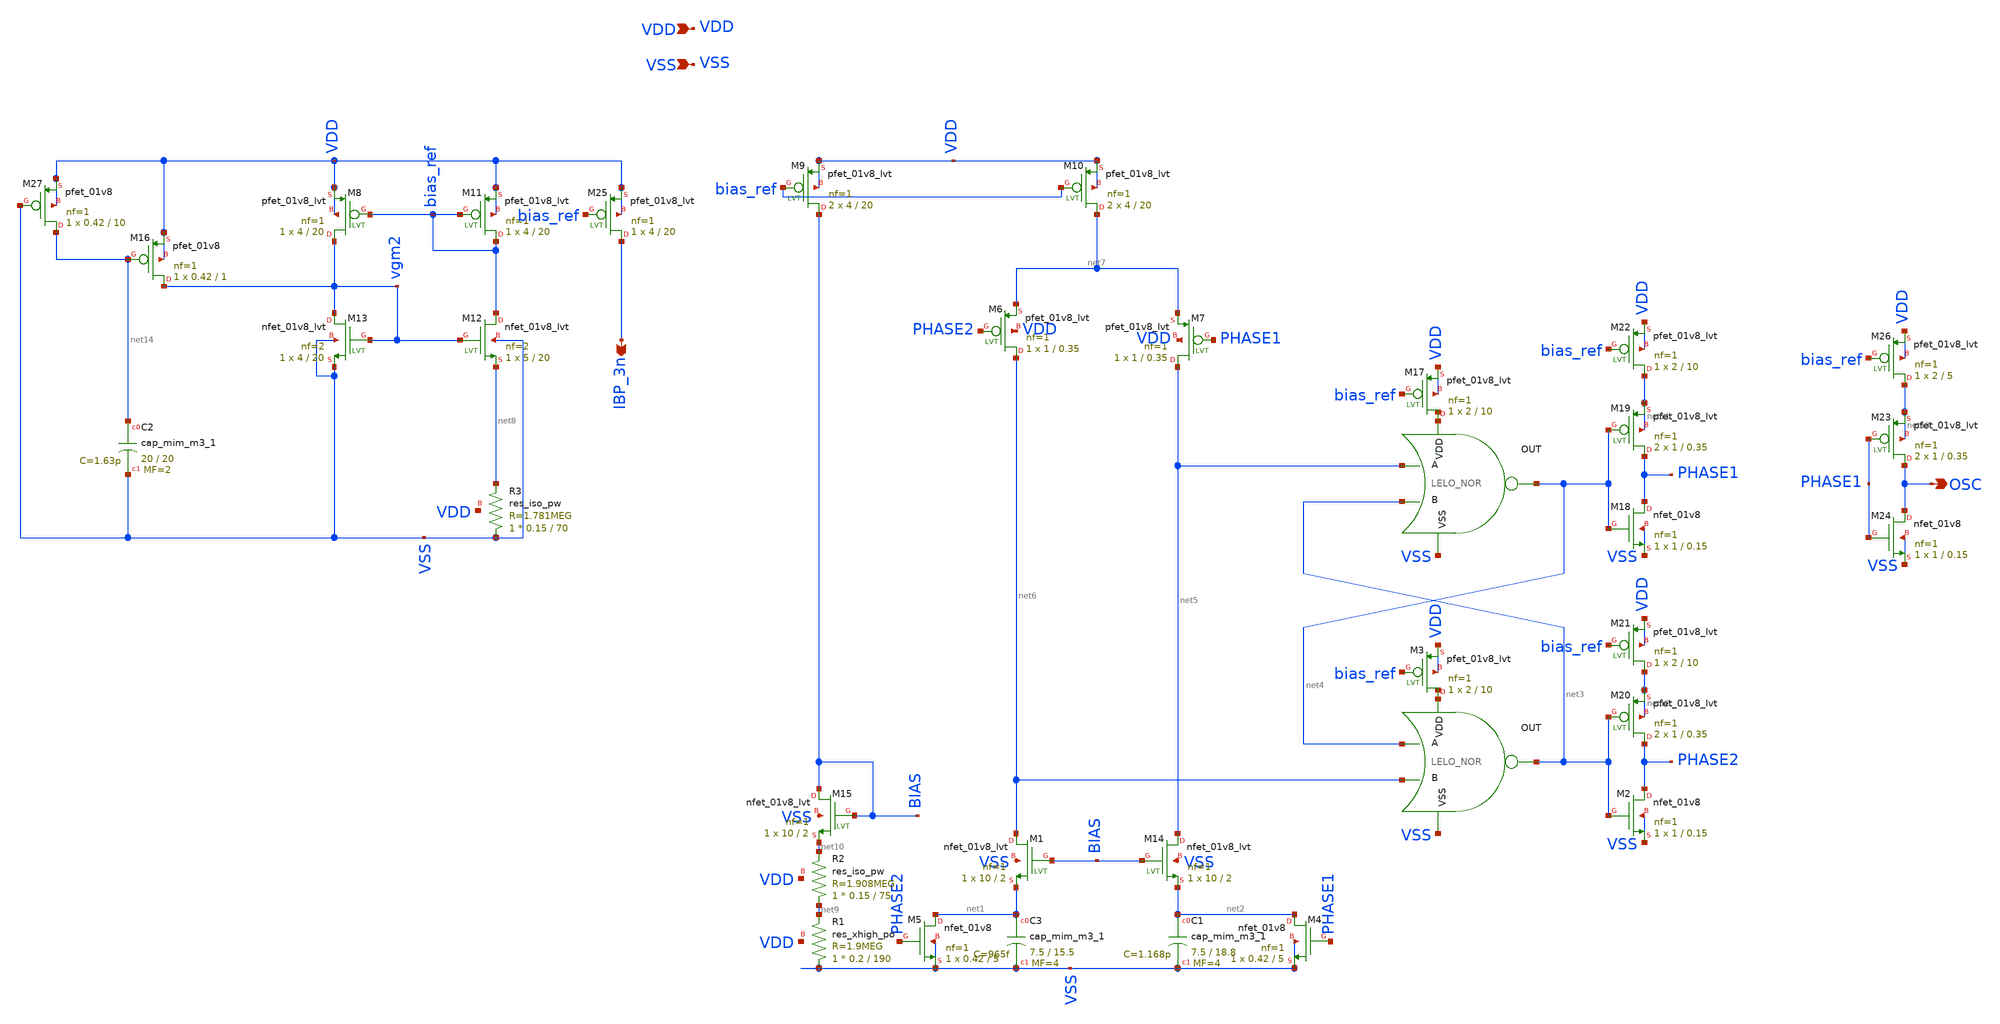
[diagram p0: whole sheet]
** sch_path: design/LELO_SVOD_SKY130A/LELO_SVOD_RELOSC.sch
**.subckt LELO_SVOD_RELOSC VDD VSS OSC IBP_3n
*.ipin VDD
*.ipin VSS
*.opin OSC
*.opin IBP_3n
x1 net15 net4 net5 net3 VSS LELO_NOR
x2 net16 net3 net4 net6 VSS LELO_NOR
XM6 net6 PHASE2 net7 VDD sky130_fd_pr__pfet_01v8_lvt L=0.35 W=1 nf=1 ad='int((1 + 1)/2) * 1 / 1 * 0.29'
+ as='int((1 + 2)/2) * 1 / 1 * 0.29' pd='2*int((1 + 1)/2) * (1 / 1 + 0.29)' ps='2*int((1 + 2)/2) * (1 / 1 + 0.29)'
+ nrd='0.29 / 1 ' nrs='0.29 / 1 ' sa=0 sb=0 sd=0 mult=1 m=1
XM7 net5 PHASE1 net7 VDD sky130_fd_pr__pfet_01v8_lvt L=0.35 W=1 nf=1 ad='int((1 + 1)/2) * 1 / 1 * 0.29'
+ as='int((1 + 2)/2) * 1 / 1 * 0.29' pd='2*int((1 + 1)/2) * (1 / 1 + 0.29)' ps='2*int((1 + 2)/2) * (1 / 1 + 0.29)'
+ nrd='0.29 / 1 ' nrs='0.29 / 1 ' sa=0 sb=0 sd=0 mult=1 m=1
XM11 bias_ref bias_ref VDD VDD sky130_fd_pr__pfet_01v8_lvt L=20 W=4 nf=1 ad='int((1 + 1)/2) * 4 / 1 * 0.29'
+ as='int((1 + 2)/2) * 4 / 1 * 0.29' pd='2*int((1 + 1)/2) * (4 / 1 + 0.29)' ps='2*int((1 + 2)/2) * (4 / 1 + 0.29)'
+ nrd='0.29 / 4 ' nrs='0.29 / 4 ' sa=0 sb=0 sd=0 mult=1 m=1
XC3 net1 VSS sky130_fd_pr__cap_mim_m3_1 W=7.5 L=15.5 MF=4 m=4
XC1 net2 VSS sky130_fd_pr__cap_mim_m3_1 W=7.5 L=18.8 MF=4 m=4
XM4 net2 PHASE1 VSS VSS sky130_fd_pr__nfet_01v8 L=5 W=0.42 nf=1 ad='int((1 + 1)/2) * 0.42 / 1 * 0.29'
+ as='int((1 + 2)/2) * 0.42 / 1 * 0.29' pd='2*int((1 + 1)/2) * (0.42 / 1 + 0.29)' ps='2*int((1 + 2)/2) * (0.42 / 1 + 0.29)'
+ nrd='0.29 / 0.42 ' nrs='0.29 / 0.42 ' sa=0 sb=0 sd=0 mult=1 m=1
XM5 net1 PHASE2 VSS VSS sky130_fd_pr__nfet_01v8 L=5 W=0.42 nf=1 ad='int((1 + 1)/2) * 0.42 / 1 * 0.29'
+ as='int((1 + 2)/2) * 0.42 / 1 * 0.29' pd='2*int((1 + 1)/2) * (0.42 / 1 + 0.29)' ps='2*int((1 + 2)/2) * (0.42 / 1 + 0.29)'
+ nrd='0.29 / 0.42 ' nrs='0.29 / 0.42 ' sa=0 sb=0 sd=0 mult=1 m=1
XM1 net6 BIAS net1 VSS sky130_fd_pr__nfet_01v8_lvt L=2 W=10 nf=1 ad='int((1 + 1)/2) * 10 / 1 * 0.29'
+ as='int((1 + 2)/2) * 10 / 1 * 0.29' pd='2*int((1 + 1)/2) * (10 / 1 + 0.29)' ps='2*int((1 + 2)/2) * (10 / 1 + 0.29)'
+ nrd='0.29 / 10 ' nrs='0.29 / 10 ' sa=0 sb=0 sd=0 mult=1 m=1
XM8 vgm2 bias_ref VDD VDD sky130_fd_pr__pfet_01v8_lvt L=20 W=4 nf=1 ad='int((1 + 1)/2) * 4 / 1 * 0.29'
+ as='int((1 + 2)/2) * 4 / 1 * 0.29' pd='2*int((1 + 1)/2) * (4 / 1 + 0.29)' ps='2*int((1 + 2)/2) * (4 / 1 + 0.29)'
+ nrd='0.29 / 4 ' nrs='0.29 / 4 ' sa=0 sb=0 sd=0 mult=1 m=1
XM12 bias_ref vgm2 net8 VSS sky130_fd_pr__nfet_01v8_lvt L=20 W=5 nf=2 ad='int((2 + 1)/2) * 5 / 2 * 0.29'
+ as='int((2 + 2)/2) * 5 / 2 * 0.29' pd='2*int((2 + 1)/2) * (5 / 2 + 0.29)' ps='2*int((2 + 2)/2) * (5 / 2 + 0.29)'
+ nrd='0.29 / 5 ' nrs='0.29 / 5 ' sa=0 sb=0 sd=0 mult=1 m=1
XM13 vgm2 vgm2 VSS VSS sky130_fd_pr__nfet_01v8_lvt L=20 W=4 nf=2 ad='int((2 + 1)/2) * 4 / 2 * 0.29' as='int((2 + 2)/2) * 4 / 2 * 0.29'
+ pd='2*int((2 + 1)/2) * (4 / 2 + 0.29)' ps='2*int((2 + 2)/2) * (4 / 2 + 0.29)' nrd='0.29 / 4 ' nrs='0.29 / 4 '
+ sa=0 sb=0 sd=0 mult=1 m=1
XM9 BIAS bias_ref VDD VDD sky130_fd_pr__pfet_01v8_lvt L=20 W=4 nf=1 ad='int((1 + 1)/2) * 4 / 1 * 0.29'
+ as='int((1 + 2)/2) * 4 / 1 * 0.29' pd='2*int((1 + 1)/2) * (4 / 1 + 0.29)' ps='2*int((1 + 2)/2) * (4 / 1 + 0.29)'
+ nrd='0.29 / 4 ' nrs='0.29 / 4 ' sa=0 sb=0 sd=0 mult=2 m=2
XM10 net7 bias_ref VDD VDD sky130_fd_pr__pfet_01v8_lvt L=20 W=4 nf=1 ad='int((1 + 1)/2) * 4 / 1 * 0.29'
+ as='int((1 + 2)/2) * 4 / 1 * 0.29' pd='2*int((1 + 1)/2) * (4 / 1 + 0.29)' ps='2*int((1 + 2)/2) * (4 / 1 + 0.29)'
+ nrd='0.29 / 4 ' nrs='0.29 / 4 ' sa=0 sb=0 sd=0 mult=2 m=2
XM14 net5 BIAS net2 VSS sky130_fd_pr__nfet_01v8_lvt L=2 W=10 nf=1 ad='int((1 + 1)/2) * 10 / 1 * 0.29'
+ as='int((1 + 2)/2) * 10 / 1 * 0.29' pd='2*int((1 + 1)/2) * (10 / 1 + 0.29)' ps='2*int((1 + 2)/2) * (10 / 1 + 0.29)'
+ nrd='0.29 / 10 ' nrs='0.29 / 10 ' sa=0 sb=0 sd=0 mult=1 m=1
XM15 BIAS BIAS net10 VSS sky130_fd_pr__nfet_01v8_lvt L=2 W=10 nf=1 ad='int((1 + 1)/2) * 10 / 1 * 0.29'
+ as='int((1 + 2)/2) * 10 / 1 * 0.29' pd='2*int((1 + 1)/2) * (10 / 1 + 0.29)' ps='2*int((1 + 2)/2) * (10 / 1 + 0.29)'
+ nrd='0.29 / 10 ' nrs='0.29 / 10 ' sa=0 sb=0 sd=0 mult=1 m=1
XM17 net17 bias_ref VDD VDD sky130_fd_pr__pfet_01v8_lvt L=10 W=2 nf=1 ad='int((1 + 1)/2) * 2 / 1 * 0.29'
+ as='int((1 + 2)/2) * 2 / 1 * 0.29' pd='2*int((1 + 1)/2) * (2 / 1 + 0.29)' ps='2*int((1 + 2)/2) * (2 / 1 + 0.29)'
+ nrd='0.29 / 2 ' nrs='0.29 / 2 ' sa=0 sb=0 sd=0 mult=1 m=1
XR3 VSS net8 VDD sky130_fd_pr__res_iso_pw W=0.15 L=70 m=1
XR1 VSS net9 VDD sky130_fd_pr__res_xhigh_po W=0.2 L=190 mult=1 m=1
XR2 net9 net10 VDD sky130_fd_pr__res_iso_pw W=0.15 L=75 m=1
XM19 PHASE1 net4 net11 net11 sky130_fd_pr__pfet_01v8_lvt L=0.35 W=1 nf=1 ad='int((1 + 1)/2) * 1 / 1 * 0.29'
+ as='int((1 + 2)/2) * 1 / 1 * 0.29' pd='2*int((1 + 1)/2) * (1 / 1 + 0.29)' ps='2*int((1 + 2)/2) * (1 / 1 + 0.29)'
+ nrd='0.29 / 1 ' nrs='0.29 / 1 ' sa=0 sb=0 sd=0 mult=2 m=2
XM20 PHASE2 net3 net12 net12 sky130_fd_pr__pfet_01v8_lvt L=0.35 W=1 nf=1 ad='int((1 + 1)/2) * 1 / 1 * 0.29'
+ as='int((1 + 2)/2) * 1 / 1 * 0.29' pd='2*int((1 + 1)/2) * (1 / 1 + 0.29)' ps='2*int((1 + 2)/2) * (1 / 1 + 0.29)'
+ nrd='0.29 / 1 ' nrs='0.29 / 1 ' sa=0 sb=0 sd=0 mult=2 m=2
XM2 PHASE2 net3 VSS VSS sky130_fd_pr__nfet_01v8 L=0.15 W=1 nf=1 ad='int((1 + 1)/2) * 1 / 1 * 0.29' as='int((1 + 2)/2) * 1 / 1 * 0.29'
+ pd='2*int((1 + 1)/2) * (1 / 1 + 0.29)' ps='2*int((1 + 2)/2) * (1 / 1 + 0.29)' nrd='0.29 / 1 ' nrs='0.29 / 1 '
+ sa=0 sb=0 sd=0 mult=1 m=1
XM18 PHASE1 net4 VSS VSS sky130_fd_pr__nfet_01v8 L=0.15 W=1 nf=1 ad='int((1 + 1)/2) * 1 / 1 * 0.29' as='int((1 + 2)/2) * 1 / 1 * 0.29'
+ pd='2*int((1 + 1)/2) * (1 / 1 + 0.29)' ps='2*int((1 + 2)/2) * (1 / 1 + 0.29)' nrd='0.29 / 1 ' nrs='0.29 / 1 '
+ sa=0 sb=0 sd=0 mult=1 m=1
XM23 OSC PHASE1 net13 net13 sky130_fd_pr__pfet_01v8_lvt L=0.35 W=1 nf=1 ad='int((1 + 1)/2) * 1 / 1 * 0.29'
+ as='int((1 + 2)/2) * 1 / 1 * 0.29' pd='2*int((1 + 1)/2) * (1 / 1 + 0.29)' ps='2*int((1 + 2)/2) * (1 / 1 + 0.29)'
+ nrd='0.29 / 1 ' nrs='0.29 / 1 ' sa=0 sb=0 sd=0 mult=2 m=2
XM24 OSC PHASE1 VSS VSS sky130_fd_pr__nfet_01v8 L=0.15 W=1 nf=1 ad='int((1 + 1)/2) * 1 / 1 * 0.29' as='int((1 + 2)/2) * 1 / 1 * 0.29'
+ pd='2*int((1 + 1)/2) * (1 / 1 + 0.29)' ps='2*int((1 + 2)/2) * (1 / 1 + 0.29)' nrd='0.29 / 1 ' nrs='0.29 / 1 '
+ sa=0 sb=0 sd=0 mult=1 m=1
XM25 IBP_3n bias_ref VDD VDD sky130_fd_pr__pfet_01v8_lvt L=20 W=4 nf=1 ad='int((1 + 1)/2) * 4 / 1 * 0.29'
+ as='int((1 + 2)/2) * 4 / 1 * 0.29' pd='2*int((1 + 1)/2) * (4 / 1 + 0.29)' ps='2*int((1 + 2)/2) * (4 / 1 + 0.29)'
+ nrd='0.29 / 4 ' nrs='0.29 / 4 ' sa=0 sb=0 sd=0 mult=1 m=1
XM3 net18 bias_ref VDD VDD sky130_fd_pr__pfet_01v8_lvt L=10 W=2 nf=1 ad='int((1 + 1)/2) * 2 / 1 * 0.29'
+ as='int((1 + 2)/2) * 2 / 1 * 0.29' pd='2*int((1 + 1)/2) * (2 / 1 + 0.29)' ps='2*int((1 + 2)/2) * (2 / 1 + 0.29)'
+ nrd='0.29 / 2 ' nrs='0.29 / 2 ' sa=0 sb=0 sd=0 mult=1 m=1
XM21 net12 bias_ref VDD VDD sky130_fd_pr__pfet_01v8_lvt L=10 W=2 nf=1 ad='int((1 + 1)/2) * 2 / 1 * 0.29'
+ as='int((1 + 2)/2) * 2 / 1 * 0.29' pd='2*int((1 + 1)/2) * (2 / 1 + 0.29)' ps='2*int((1 + 2)/2) * (2 / 1 + 0.29)'
+ nrd='0.29 / 2 ' nrs='0.29 / 2 ' sa=0 sb=0 sd=0 mult=1 m=1
XM22 net11 bias_ref VDD VDD sky130_fd_pr__pfet_01v8_lvt L=10 W=2 nf=1 ad='int((1 + 1)/2) * 2 / 1 * 0.29'
+ as='int((1 + 2)/2) * 2 / 1 * 0.29' pd='2*int((1 + 1)/2) * (2 / 1 + 0.29)' ps='2*int((1 + 2)/2) * (2 / 1 + 0.29)'
+ nrd='0.29 / 2 ' nrs='0.29 / 2 ' sa=0 sb=0 sd=0 mult=1 m=1
XM26 net13 bias_ref VDD VDD sky130_fd_pr__pfet_01v8_lvt L=5 W=2 nf=1 ad='int((1 + 1)/2) * 2 / 1 * 0.29'
+ as='int((1 + 2)/2) * 2 / 1 * 0.29' pd='2*int((1 + 1)/2) * (2 / 1 + 0.29)' ps='2*int((1 + 2)/2) * (2 / 1 + 0.29)'
+ nrd='0.29 / 2 ' nrs='0.29 / 2 ' sa=0 sb=0 sd=0 mult=1 m=1
XM16 vgm2 net14 VDD VDD sky130_fd_pr__pfet_01v8 L=1 W=0.42 nf=1 ad='int((1 + 1)/2) * 0.42 / 1 * 0.29'
+ as='int((1 + 2)/2) * 0.42 / 1 * 0.29' pd='2*int((1 + 1)/2) * (0.42 / 1 + 0.29)' ps='2*int((1 + 2)/2) * (0.42 / 1 + 0.29)'
+ nrd='0.29 / 0.42 ' nrs='0.29 / 0.42 ' sa=0 sb=0 sd=0 mult=1 m=1
XM27 net14 VSS VDD VDD sky130_fd_pr__pfet_01v8 L=10 W=0.42 nf=1 ad='int((1 + 1)/2) * 0.42 / 1 * 0.29'
+ as='int((1 + 2)/2) * 0.42 / 1 * 0.29' pd='2*int((1 + 1)/2) * (0.42 / 1 + 0.29)' ps='2*int((1 + 2)/2) * (0.42 / 1 + 0.29)'
+ nrd='0.29 / 0.42 ' nrs='0.29 / 0.42 ' sa=0 sb=0 sd=0 mult=1 m=1
XC2 net14 VSS sky130_fd_pr__cap_mim_m3_1 W=20 L=20 MF=2 m=2
**.ends

* expanding   symbol:  LELO_SVOD_SKY130A/LELO_NOR.sym # of pins=5
** sym_path: design/LELO_SVOD_SKY130A/LELO_NOR.sym
** sch_path: design/LELO_SVOD_SKY130A/LELO_NOR.sch
.subckt LELO_NOR VDD OUT A B VSS
*.ipin VDD
*.ipin VSS
*.opin OUT
*.ipin A
*.ipin B
XM2 OUT B VSS VSS sky130_fd_pr__nfet_01v8 L=0.15 W=2 nf=1 ad='int((1 + 1)/2) * 2 / 1 * 0.29' as='int((1 + 2)/2) * 2 / 1 * 0.29'
+ pd='2*int((1 + 1)/2) * (2 / 1 + 0.29)' ps='2*int((1 + 2)/2) * (2 / 1 + 0.29)' nrd='0.29 / 2 ' nrs='0.29 / 2 '
+ sa=0 sb=0 sd=0 mult=1 m=1
XM1 OUT A VSS VSS sky130_fd_pr__nfet_01v8 L=0.15 W=2 nf=1 ad='int((1 + 1)/2) * 2 / 1 * 0.29' as='int((1 + 2)/2) * 2 / 1 * 0.29'
+ pd='2*int((1 + 1)/2) * (2 / 1 + 0.29)' ps='2*int((1 + 2)/2) * (2 / 1 + 0.29)' nrd='0.29 / 2 ' nrs='0.29 / 2 '
+ sa=0 sb=0 sd=0 mult=1 m=1
XM3 OUT B net1 VDD sky130_fd_pr__pfet_01v8 L=0.15 W=4 nf=1 ad='int((1 + 1)/2) * 4 / 1 * 0.29' as='int((1 + 2)/2) * 4 / 1 * 0.29'
+ pd='2*int((1 + 1)/2) * (4 / 1 + 0.29)' ps='2*int((1 + 2)/2) * (4 / 1 + 0.29)' nrd='0.29 / 4 ' nrs='0.29 / 4 '
+ sa=0 sb=0 sd=0 mult=1 m=1
XM4 net1 A VDD VDD sky130_fd_pr__pfet_01v8 L=0.15 W=4 nf=1 ad='int((1 + 1)/2) * 4 / 1 * 0.29' as='int((1 + 2)/2) * 4 / 1 * 0.29'
+ pd='2*int((1 + 1)/2) * (4 / 1 + 0.29)' ps='2*int((1 + 2)/2) * (4 / 1 + 0.29)' nrd='0.29 / 4 ' nrs='0.29 / 4 '
+ sa=0 sb=0 sd=0 mult=1 m=1
.ends

.end
